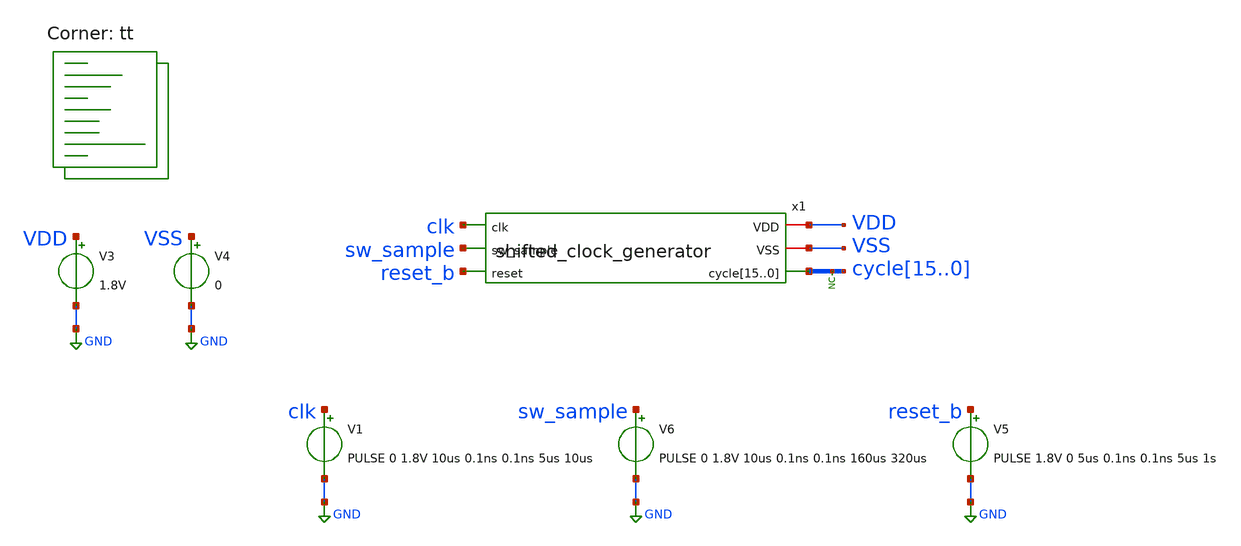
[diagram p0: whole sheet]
** sch_path: xschem/tests/shifted_clock_generator/shifted_clock_generator_test.sch
**.subckt shifted_clock_generator_test
V3 VDD GND 1.8V
V4 VSS GND 0
* noconn cycle[15..0]
V1 clk GND PULSE 0 1.8V 10us 0.1ns 0.1ns 5us 10us
V5 reset_b GND PULSE 1.8V 0 5us 0.1ns 0.1ns 5us 1s
x1 VDD clk sw_sample VSS reset_b cycle15 cycle14 cycle13 cycle12 cycle11 cycle10 cycle9 cycle8
+ cycle7 cycle6 cycle5 cycle4 cycle3 cycle2 cycle1 cycle0 shifted_clock_generator
V6 sw_sample GND PULSE 0 1.8V 10us 0.1ns 0.1ns 160us 320us
**** begin user architecture code
 *.lib $::SKYWATER_MODELS/sky130.lib.spice tt
.include $::SKYWATER_STDCELLS/sky130_fd_sc_hd.spice


.options acct list
.temp 25
*vvcc VDD 0 dc 1.8
*vvss VSS 0 0
.control
save all
tran 0.1u 400u
*plot RST_PLS clk+2 Pulse+4
plot reset_b-6 clk-4 sw_sample-2 cycle0 cycle1+2 cycle2+4 cycle3+6 cycle4+8 cycle5+10 cycle6+12
+ cycle7+14 cycle8+16 cycle9+18 cycle10+20 cycle11+22 cycle12+24 cycle13+26 cycle14+28 cycle15+30

write shifted_clock_generator_test.raw
.endc


.lib $::SKYWATER_MODELS/sky130.lib.spice tt
**** end user architecture code
**.ends

* expanding   symbol:  src/shifted_clock_generator/shifted_clock_generator.sym # of pins=6
** sym_path: xschem/src/shifted_clock_generator/shifted_clock_generator.sym
** sch_path: xschem/src/shifted_clock_generator/shifted_clock_generator.sch
.subckt shifted_clock_generator VDD clk sw_sample VSS reset cycle15 cycle14 cycle13 cycle12 cycle11
+ cycle10 cycle9 cycle8 cycle7 cycle6 cycle5 cycle4 cycle3 cycle2 cycle1 cycle0
*.opin
*+ cycle15,cycle14,cycle13,cycle12,cycle11,cycle10,cycle9,cycle8,cycle7,cycle6,cycle5,cycle4,cycle3,cycle2,cycle1,cycle0
*.iopin VSS
*.iopin VDD
*.ipin clk
*.ipin reset
*.ipin sw_sample
x32 net16 net17 net33 VSS VSS VDD VDD net4 sky130_fd_sc_hd__dfrtp_1
x1 net5 net4 net18 VSS VSS VDD VDD net31 sky130_fd_sc_hd__dfrtp_1
x2 net6 net31 net19 VSS VSS VDD VDD net32 sky130_fd_sc_hd__dfrtp_1
x3 net7 net32 net20 VSS VSS VDD VDD cycle4 sky130_fd_sc_hd__dfrtp_1
x4 net8 cycle4 net21 VSS VSS VDD VDD cycle5 sky130_fd_sc_hd__dfrtp_1
x5 net9 cycle5 net22 VSS VSS VDD VDD cycle6 sky130_fd_sc_hd__dfrtp_1
x6 net10 cycle6 net23 VSS VSS VDD VDD cycle7 sky130_fd_sc_hd__dfrtp_1
x7 net11 cycle7 net24 VSS VSS VDD VDD cycle8 sky130_fd_sc_hd__dfrtp_1
x8 net12 cycle8 net25 VSS VSS VDD VDD cycle9 sky130_fd_sc_hd__dfrtp_1
x9 net13 cycle9 net26 VSS VSS VDD VDD cycle10 sky130_fd_sc_hd__dfrtp_1
x10 net14 cycle10 net27 VSS VSS VDD VDD cycle11 sky130_fd_sc_hd__dfrtp_1
x11 net15 cycle11 net28 VSS VSS VDD VDD cycle12 sky130_fd_sc_hd__dfrtp_1
x12 net3 cycle12 net29 VSS VSS VDD VDD cycle13 sky130_fd_sc_hd__dfrtp_1
x13 net1 cycle13 net34 VSS VSS VDD VDD cycle14 sky130_fd_sc_hd__dfrtp_1
x14 net2 cycle14 net30 VSS VSS VDD VDD cycle15 sky130_fd_sc_hd__dfrtp_1
x31 net35 net36 net37 VSS VSS VDD VDD net17 sky130_fd_sc_hd__dfrtp_1
x37 net39 VSS VSS VDD VDD reset_b sky130_fd_sc_hd__buf_16
x35 net38 reset VSS VSS VDD VDD net39 sky130_fd_sc_hd__and2_4
x15 net17 VSS VSS VDD VDD cycle0 sky130_fd_sc_hd__buf_1
x16 net48 VSS VSS VDD VDD net40 sky130_fd_sc_hd__buf_2
x20 net48 VSS VSS VDD VDD net41 sky130_fd_sc_hd__buf_2
x21 net48 VSS VSS VDD VDD net42 sky130_fd_sc_hd__buf_2
x22 net48 VSS VSS VDD VDD net43 sky130_fd_sc_hd__buf_2
x23 net49 VSS VSS VDD VDD net44 sky130_fd_sc_hd__buf_2
x24 net49 VSS VSS VDD VDD net45 sky130_fd_sc_hd__buf_2
x25 net49 VSS VSS VDD VDD net46 sky130_fd_sc_hd__buf_2
x26 net49 VSS VSS VDD VDD net47 sky130_fd_sc_hd__buf_2
x27 clk VSS VSS VDD VDD net48 sky130_fd_sc_hd__buf_4
x28 clk VSS VSS VDD VDD net49 sky130_fd_sc_hd__buf_4
x17 net40 VSS VSS VDD VDD net35 sky130_fd_sc_hd__buf_1
x18 net40 VSS VSS VDD VDD net16 sky130_fd_sc_hd__buf_1
x19 net41 VSS VSS VDD VDD net5 sky130_fd_sc_hd__buf_1
x29 net41 VSS VSS VDD VDD net6 sky130_fd_sc_hd__buf_1
x30 net42 VSS VSS VDD VDD net7 sky130_fd_sc_hd__buf_1
x33 net42 VSS VSS VDD VDD net8 sky130_fd_sc_hd__buf_1
x47 net43 VSS VSS VDD VDD net9 sky130_fd_sc_hd__buf_1
x48 net43 VSS VSS VDD VDD net10 sky130_fd_sc_hd__buf_1
x51 net44 VSS VSS VDD VDD net11 sky130_fd_sc_hd__buf_1
x52 net44 VSS VSS VDD VDD net12 sky130_fd_sc_hd__buf_1
x53 net45 VSS VSS VDD VDD net13 sky130_fd_sc_hd__buf_1
x54 net45 VSS VSS VDD VDD net14 sky130_fd_sc_hd__buf_1
x55 net46 VSS VSS VDD VDD net15 sky130_fd_sc_hd__buf_1
x56 net46 VSS VSS VDD VDD net3 sky130_fd_sc_hd__buf_1
x57 net47 VSS VSS VDD VDD net1 sky130_fd_sc_hd__buf_1
x58 net47 VSS VSS VDD VDD net2 sky130_fd_sc_hd__buf_1
x62 net4 VSS VSS VDD VDD cycle1 sky130_fd_sc_hd__buf_1
x66 net31 VSS VSS VDD VDD cycle2 sky130_fd_sc_hd__buf_1
x70 net32 VSS VSS VDD VDD cycle3 sky130_fd_sc_hd__buf_1
x74 reset_b VSS VSS VDD VDD net37 sky130_fd_sc_hd__buf_1
x75 reset_b VSS VSS VDD VDD net33 sky130_fd_sc_hd__buf_1
x76 reset_b VSS VSS VDD VDD net18 sky130_fd_sc_hd__buf_1
x77 reset_b VSS VSS VDD VDD net19 sky130_fd_sc_hd__buf_1
x78 reset_b VSS VSS VDD VDD net20 sky130_fd_sc_hd__buf_1
x79 reset_b VSS VSS VDD VDD net21 sky130_fd_sc_hd__buf_1
x80 reset_b VSS VSS VDD VDD net22 sky130_fd_sc_hd__buf_1
x81 reset_b VSS VSS VDD VDD net23 sky130_fd_sc_hd__buf_1
x82 reset_b VSS VSS VDD VDD net24 sky130_fd_sc_hd__buf_1
x83 reset_b VSS VSS VDD VDD net25 sky130_fd_sc_hd__buf_1
x84 reset_b VSS VSS VDD VDD net26 sky130_fd_sc_hd__buf_1
x85 reset_b VSS VSS VDD VDD net27 sky130_fd_sc_hd__buf_1
x86 reset_b VSS VSS VDD VDD net28 sky130_fd_sc_hd__buf_1
x87 reset_b VSS VSS VDD VDD net29 sky130_fd_sc_hd__buf_1
x88 reset_b VSS VSS VDD VDD net34 sky130_fd_sc_hd__buf_1
x89 reset_b VSS VSS VDD VDD net30 sky130_fd_sc_hd__buf_1
x34 sw_sample VSS VSS VDD VDD net38 sky130_fd_sc_hd__inv_1
x36 VDD VSS VSS VDD VDD net36 sky130_fd_sc_hd__buf_1
.ends

.GLOBAL GND
.end
